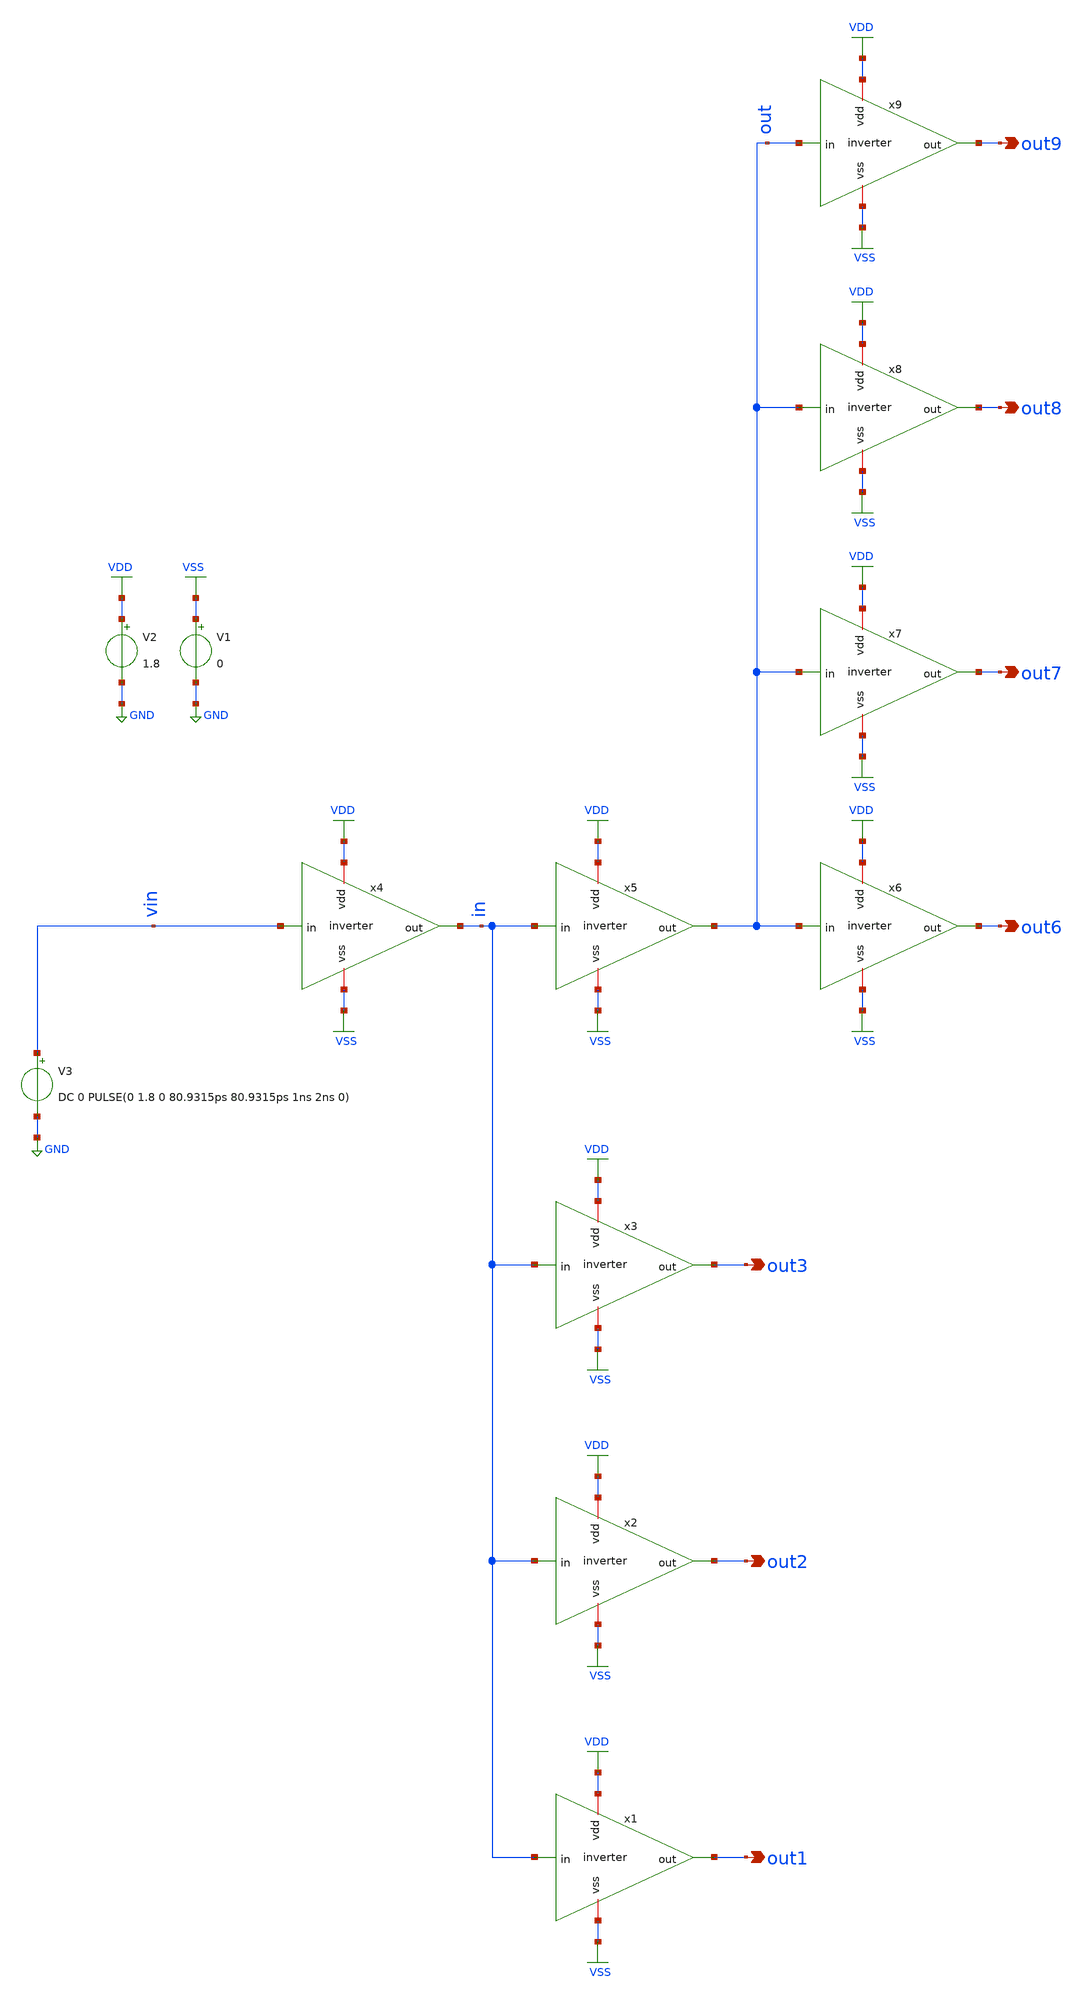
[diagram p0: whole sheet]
** sch_path: scripts/fo4/tb_optimal_w_tt.sch
**.subckt tb_optimal_w_tt out7 out6 out8 out9 out3 out2 out1
*.opin out7
*.opin out6
*.opin out8
*.opin out9
*.opin out3
*.opin out2
*.opin out1
V1 VSS GND 0
V2 VDD GND 1.8
V3 vin GND DC 0 PULSE(0 1.8 0 80.9315ps 80.9315ps 1ns 2ns 0)

x1 VDD out1 in VSS inverter
x2 VDD out2 in VSS inverter
x3 VDD out3 in VSS inverter
x4 VDD in vin VSS inverter
x5 VDD out in VSS inverter
x6 VDD out6 out VSS inverter
x7 VDD out7 out VSS inverter
x8 VDD out8 out VSS inverter
x9 VDD out9 out VSS inverter
**** begin user architecture code



.param pp = 2.81
.param pn = 0.88

********************************
* Control section
********************************
.control

* Voltage values to calculate rise and fall times
let v_steady = 1.8
let per10 = v_steady * 0.1
let per90 = v_steady * 0.9
let per50 = v_steady * 0.5

* Run transient analysis
TRAN 1p 6n $ 3 periods

* Find rise and fall times
echo
meas  TRAN  t_rise  TRIG  v(out) VAL=per10 RISE=2  TARG v(out)  VAL=per90 RISE=2
meas  TRAN  t_fall  TRIG  v(out) VAL=per90 FALL=2  TARG v(out)  VAL=per10 FALL=2
echo
echo ********************************** End of Simulation **********************************
echo

* Export vector data into raw file
* write data_VACIO.raw wnv wpv trv tfv

* Plot both rise and fall times vs. NMOS widths
plot out in
.endc






.lib $::SKYWATER_MODELS/sky130.lib.spice lh

.param mc_mm_switch=0
.param mc_pr_switch=1


**** end user architecture code
**.ends

* expanding   symbol:  inverter.sym # of pins=4
** sym_path: scripts/fo4/inverter.sym
** sch_path: scripts/fo4/inverter.sch
.subckt inverter vdd out in vss
*.opin out
*.ipin in
*.iopin vdd
*.iopin vss
XM1 out in vdd vdd sky130_fd_pr__pfet_01v8 L=0.15 W=pp nf=1 ad='int((nf+1)/2) * W/nf * 0.29' as='int((nf+2)/2) * W/nf * 0.29'
+ pd='2*int((nf+1)/2) * (W/nf + 0.29)' ps='2*int((nf+2)/2) * (W/nf + 0.29)' nrd='0.29 / W' nrs='0.29 / W'
+ sa=0 sb=0 sd=0 mult=1 m=1
XM2 out in vss vss sky130_fd_pr__nfet_01v8 L=0.15 W=pn nf=1 ad='int((nf+1)/2) * W/nf * 0.29' as='int((nf+2)/2) * W/nf * 0.29'
+ pd='2*int((nf+1)/2) * (W/nf + 0.29)' ps='2*int((nf+2)/2) * (W/nf + 0.29)' nrd='0.29 / W' nrs='0.29 / W'
+ sa=0 sb=0 sd=0 mult=1 m=1
.ends

.GLOBAL VSS
.GLOBAL VDD
.GLOBAL GND
.end
